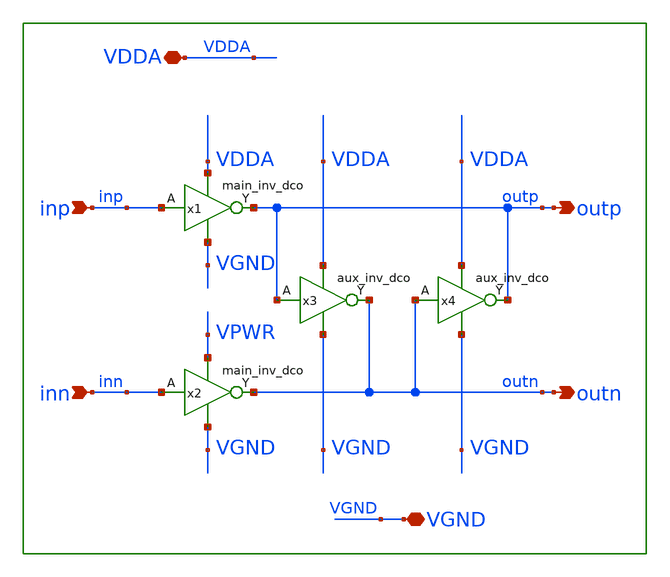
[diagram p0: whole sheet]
** sch_path: xschem/lib/cc_inv_dco.sch
**.subckt cc_inv_dco outp inn VGND outn inp VDDA
*.opin outp
*.ipin inn
*.iopin VGND
*.opin outn
*.ipin inp
*.iopin VDDA
x1 VDDA VGND outp inp main_inv_dco
x2 VPWR VGND outn inn main_inv_dco
x3 outp outn VDDA VGND aux_inv_dco
x4 outn outp VDDA VGND aux_inv_dco
**.ends

* expanding   symbol:  ../lib/main_inv_dco.sym # of pins=4
** sym_path: xschem/lib/main_inv_dco.sym
** sch_path: xschem/lib/main_inv_dco.sch
.subckt main_inv_dco VDDA VGND Y A
*.iopin VDDA
*.iopin VGND
*.ipin A
*.opin Y
XM3 Y A VGND VGND sky130_fd_pr__nfet_01v8 L=1.2 W=4 nf=2 ad='int((nf+1)/2) * W/nf * 0.29' as='int((nf+2)/2) * W/nf * 0.29'
+ pd='2*int((nf+1)/2) * (W/nf + 0.29)' ps='2*int((nf+2)/2) * (W/nf + 0.29)' nrd='0.29 / W' nrs='0.29 / W'
+ sa=0 sb=0 sd=0 mult=1 m=1
XM2 Y A VDDA VDDA sky130_fd_pr__pfet_01v8 L=1.2 W=6 nf=2 ad='int((nf+1)/2) * W/nf * 0.29' as='int((nf+2)/2) * W/nf * 0.29'
+ pd='2*int((nf+1)/2) * (W/nf + 0.29)' ps='2*int((nf+2)/2) * (W/nf + 0.29)' nrd='0.29 / W' nrs='0.29 / W'
+ sa=0 sb=0 sd=0 mult=1 m=1
.ends


* expanding   symbol:  ../lib/aux_inv_dco.sym # of pins=4
** sym_path: xschem/lib/aux_inv_dco.sym
** sch_path: xschem/lib/aux_inv_dco.sch
.subckt aux_inv_dco A Y VDDA VGND
*.iopin VDDA
*.iopin VGND
*.ipin A
*.opin Y
XM3 Y A VGND VGND sky130_fd_pr__nfet_01v8 L=1.2 W=2 nf=1 ad='int((nf+1)/2) * W/nf * 0.29' as='int((nf+2)/2) * W/nf * 0.29'
+ pd='2*int((nf+1)/2) * (W/nf + 0.29)' ps='2*int((nf+2)/2) * (W/nf + 0.29)' nrd='0.29 / W' nrs='0.29 / W'
+ sa=0 sb=0 sd=0 mult=1 m=1
XM2 Y A VDDA VDDA sky130_fd_pr__pfet_01v8 L=1.2 W=3 nf=1 ad='int((nf+1)/2) * W/nf * 0.29' as='int((nf+2)/2) * W/nf * 0.29'
+ pd='2*int((nf+1)/2) * (W/nf + 0.29)' ps='2*int((nf+2)/2) * (W/nf + 0.29)' nrd='0.29 / W' nrs='0.29 / W'
+ sa=0 sb=0 sd=0 mult=1 m=1
.ends

.end
